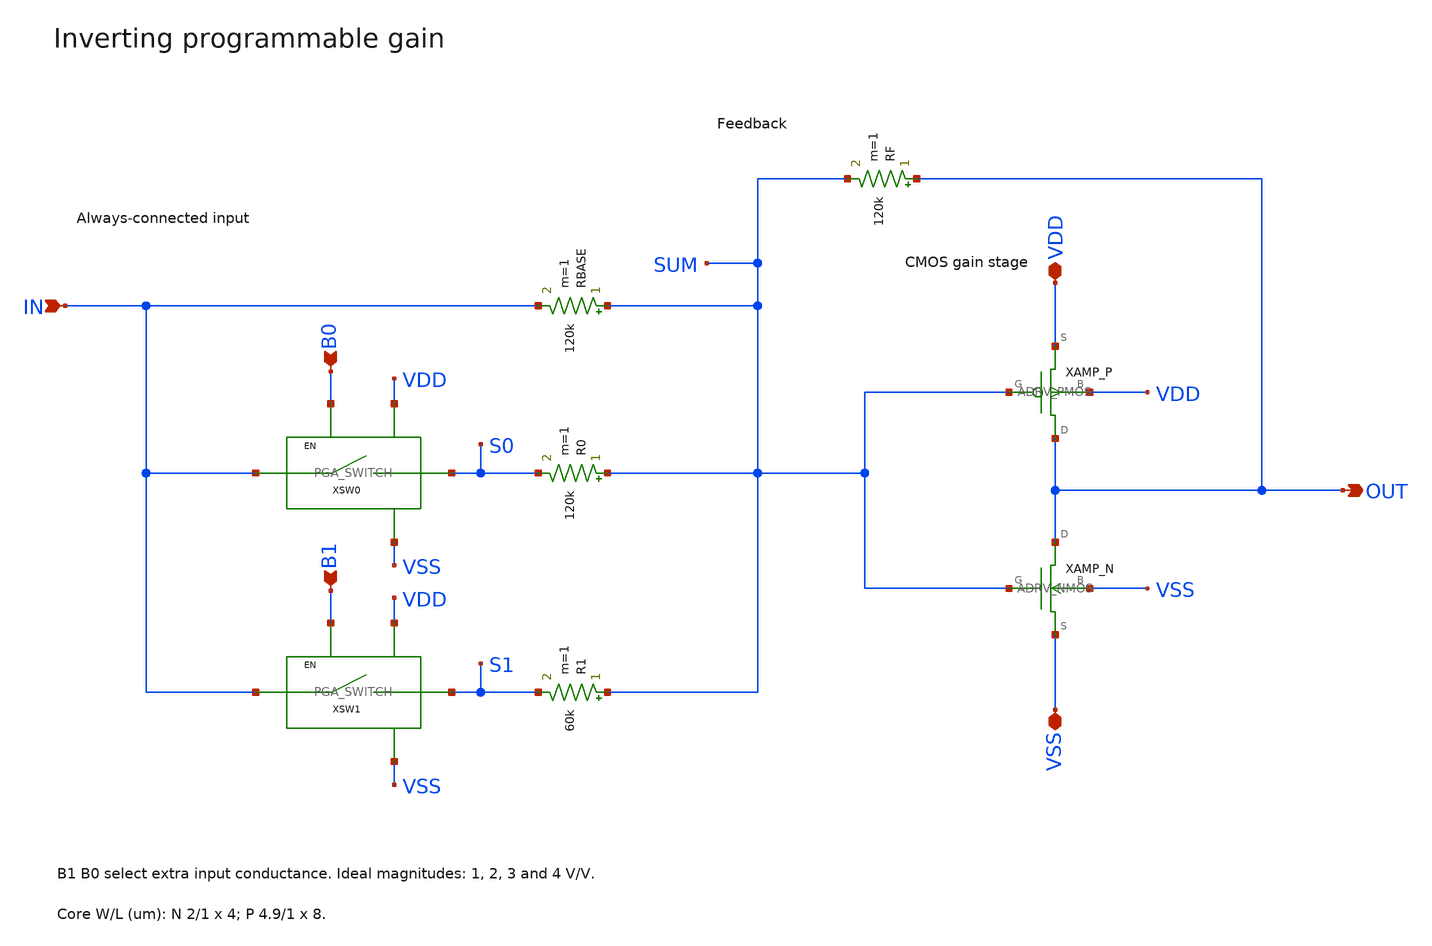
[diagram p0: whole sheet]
** sch_path: examples/sky130-programmable-gain/PGA_STAGE.sch
**.subckt PGA_STAGE IN OUT VDD VSS B0 B1
*.ipin IN
*.opin OUT
*.iopin VDD
*.iopin VSS
*.ipin B0
*.ipin B1
RBASE SUM IN 120k m=1
R0 SUM S0 120k m=1
R1 SUM S1 60k m=1
RF OUT SUM 120k m=1
XAMP_P OUT SUM VDD VDD sky130_fd_pr__pfet_01v8 w=4.9 l=1 nf=1 ad=1.47 as=1.47 pd=10.4 ps=10.4 m=8
XAMP_N OUT SUM VSS VSS sky130_fd_pr__nfet_01v8 w=2 l=1 nf=1 ad=0.6 as=0.6 pd=4.6 ps=4.6 m=4
XSW0 IN S0 B0 VDD VSS PGA_SWITCH
XSW1 IN S1 B1 VDD VSS PGA_SWITCH
**.ends

* expanding   symbol:  PGA_SWITCH.sym # of pins=5
** sym_path: examples/sky130-programmable-gain/PGA_SWITCH.sym
** sch_path: examples/sky130-programmable-gain/PGA_SWITCH.sch
.subckt PGA_SWITCH A B EN VDD VSS
*.ipin EN
*.iopin VDD
*.iopin VSS
*.iopin A
*.iopin B
XIP ENB EN VDD VDD sky130_fd_pr__pfet_01v8 w=1.2 l=0.15 nf=1 ad=0.36 as=0.36 pd=3 ps=3 m=1
XIN ENB EN VSS VSS sky130_fd_pr__nfet_01v8 w=0.6 l=0.15 nf=1 ad=0.18 as=0.18 pd=1.8 ps=1.8 m=1
XTN B EN A VSS sky130_fd_pr__nfet_01v8 w=2 l=0.15 nf=1 ad=0.6 as=0.6 pd=4.6 ps=4.6 m=1
XTP B ENB A VDD sky130_fd_pr__pfet_01v8 w=4 l=0.15 nf=1 ad=1.2 as=1.2 pd=8.6 ps=8.6 m=1
.ends

.end
